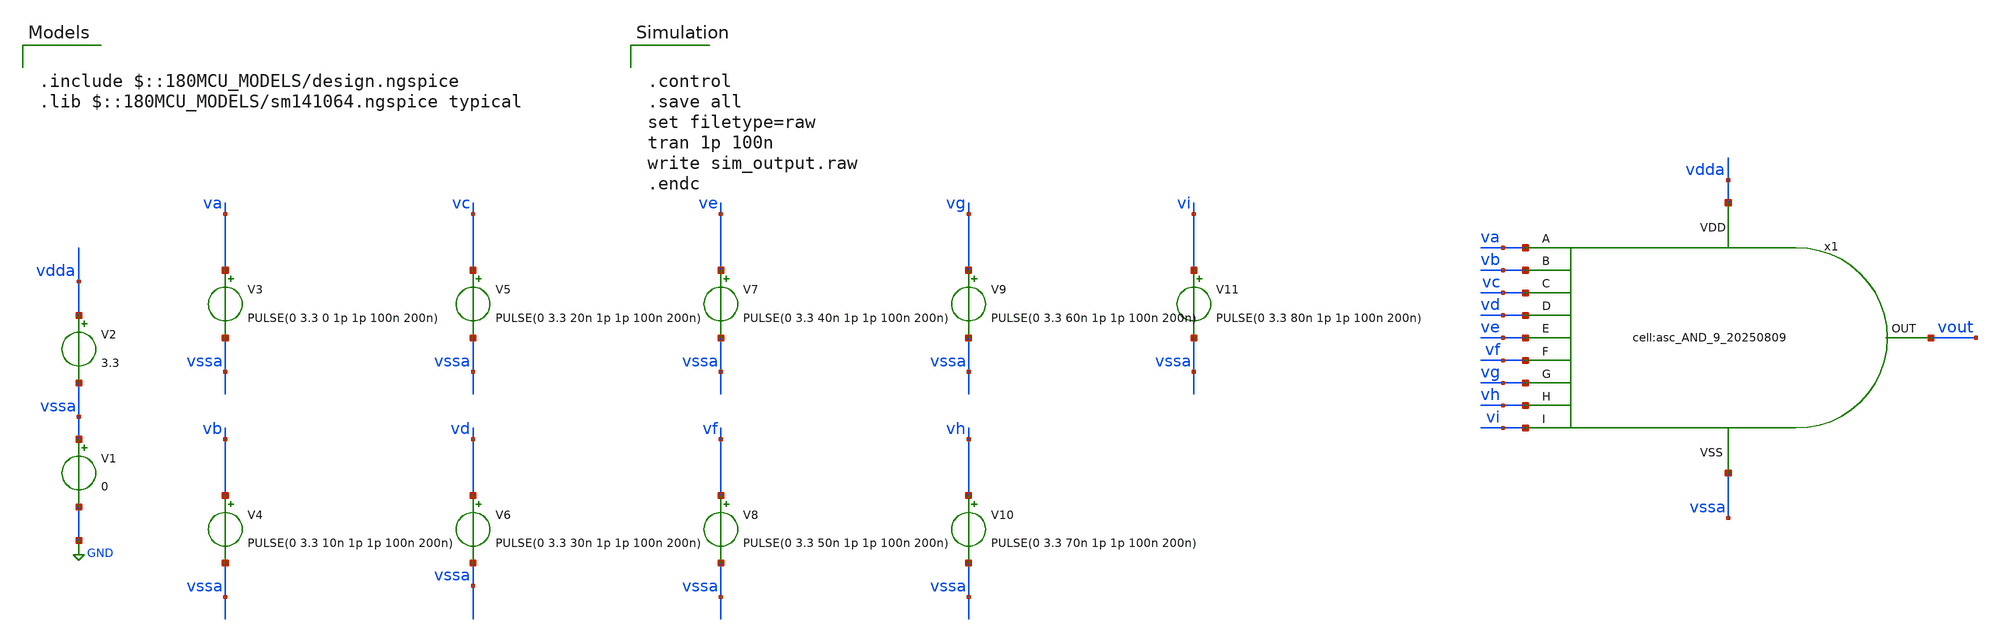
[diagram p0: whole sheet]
** sch_path: designs/libs/tb_analog/tb_asc_AND_9/tb_asc_AND_9.sch
**.subckt tb_asc_AND_9
V1 vssa GND 0
V2 vdda vssa 3.3
V3 va vssa PULSE(0 3.3 0 1p 1p 100n 200n)
V4 vb vssa PULSE(0 3.3 10n 1p 1p 100n 200n)
V5 vc vssa PULSE(0 3.3 20n 1p 1p 100n 200n)
V7 ve vssa PULSE(0 3.3 40n 1p 1p 100n 200n)
V9 vg vssa PULSE(0 3.3 60n 1p 1p 100n 200n)
V11 vi vssa PULSE(0 3.3 80n 1p 1p 100n 200n)
V6 vd vssa PULSE(0 3.3 30n 1p 1p 100n 200n)
V8 vf vssa PULSE(0 3.3 50n 1p 1p 100n 200n)
V10 vh vssa PULSE(0 3.3 70n 1p 1p 100n 200n)
x1 vdda vssa vout va vb vc vd ve vf vg vh vi asc_AND_9_20250809
**** begin user architecture code

.include $::180MCU_MODELS/design.ngspice
.lib $::180MCU_MODELS/sm141064.ngspice typical



.control
.save all
set filetype=raw
tran 1p 100n
write sim_output.raw
.endc


**** end user architecture code
**.ends
.GLOBAL GND
.end
